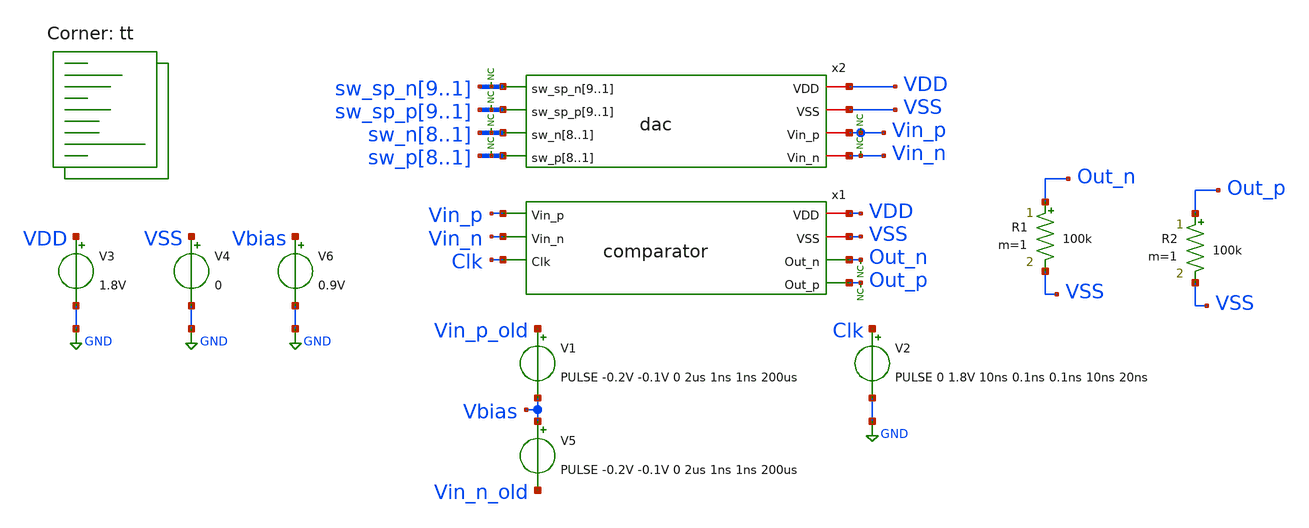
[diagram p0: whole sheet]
** sch_path: xschem/tests/comparator/comparator_fast_cap_loaded_input_test.sch
**.subckt comparator_fast_cap_loaded_input_test
V3 VDD GND 1.8V
V4 VSS GND 0
x1 VDD VSS Vin_p Out_n Vin_n Out_p Clk comparator
V1 Vin_p_old Vbias PULSE -0.2V -0.1V 0 2us 1ns 1ns 200us
V2 Clk GND PULSE 0 1.8V 10ns 0.1ns 0.1ns 10ns 20ns
* noconn Out_p
* noconn Out_n
V5 Vbias Vin_n_old PULSE -0.2V -0.1V 0 2us 1ns 1ns 200us
V6 Vbias GND 0.9V
R1 Out_n VSS 100k m=1
R2 Out_p VSS 100k m=1
x2 sw_sp_n9 sw_sp_n8 sw_sp_n7 sw_sp_n6 sw_sp_n5 sw_sp_n4 sw_sp_n3 sw_sp_n2 sw_sp_n1 VDD sw_sp_p9
+ sw_sp_p8 sw_sp_p7 sw_sp_p6 sw_sp_p5 sw_sp_p4 sw_sp_p3 sw_sp_p2 sw_sp_p1 VSS sw_n8 sw_n7 sw_n6 sw_n5 sw_n4
+ sw_n3 sw_n2 sw_n1 Vin_p sw_p8 sw_p7 sw_p6 sw_p5 sw_p4 sw_p3 sw_p2 sw_p1 Vin_n dac
* noconn sw_sp_n[9..1]
* noconn sw_sp_p[9..1]
* noconn sw_n[8..1]
* noconn sw_p[8..1]
* noconn Vin_p
* noconn Vin_n
**** begin user architecture code
 *.lib $::SKYWATER_MODELS/sky130.lib.spice tt
.include $::SKYWATER_STDCELLS/sky130_fd_sc_hd.spice


.options acct list

v_sp_n1 sw_sp_n1 gnd  PULSE(0 1.8V 0 0.1ns 0.1ns 15ns 200us)
v_sp_n2 sw_sp_n2 gnd  0
v_sp_n3 sw_sp_n3 gnd  0
v_sp_n4 sw_sp_n4 gnd  0
v_sp_n5 sw_sp_n5 gnd  0
v_sp_n6 sw_sp_n6 gnd  0
v_sp_n7 sw_sp_n7 gnd  0
v_sp_n8 sw_sp_n8 gnd  0
v_sp_n9 sw_sp_n9 gnd  0

v_n1 sw_n1 gnd  1.8V
v_n2 sw_n2 gnd  1.8V
v_n3 sw_n3 gnd  1.8V
v_n4 sw_n4 gnd  1.8V
v_n5 sw_n5 gnd  1.8V
v_n6 sw_n6 gnd  1.8V
v_n7 sw_n7 gnd  1.8V
v_n8 sw_n8 gnd  1.8V

v_sp_p1 sw_sp_p1 gnd  0
v_sp_p2 sw_sp_p2 gnd  0
v_sp_p3 sw_sp_p3 gnd  0
v_sp_p4 sw_sp_p4 gnd  0
v_sp_p5 sw_sp_p5 gnd  0
v_sp_p6 sw_sp_p6 gnd  0
v_sp_p7 sw_sp_p7 gnd  0
v_sp_p8 sw_sp_p8 gnd  0
v_sp_p9 sw_sp_p9 gnd  0

v_p1 sw_p1 gnd  1.8V
v_p2 sw_p2 gnd  1.8V
v_p3 sw_p3 gnd  1.8V
v_p4 sw_p4 gnd  1.8V
v_p5 sw_p5 gnd  1.8V
v_p6 sw_p6 gnd  1.8V
v_p7 sw_p7 gnd  1.8V
v_p8 sw_p8 gnd  1.8V

.temp 25
.control
save all
tran 0.1n 50n uic
ic v(vin_p)=0.7 v(vin_n)=1.1
*dc V1 0 1.8V 0.1
plot Vin_p-Vin_n Out_p-Out_n Clk-4
plot Vin_p-Vin_n x1.pre_amp_p-x1.pre_amp_n Clk-4
plot x1.pre_amp_p x1.pre_amp_n vin_p vin_n
*write comparator_fast_test.raw
.endc


.lib $::SKYWATER_MODELS/sky130.lib.spice tt
**** end user architecture code
**.ends
.GLOBAL GND
.end
